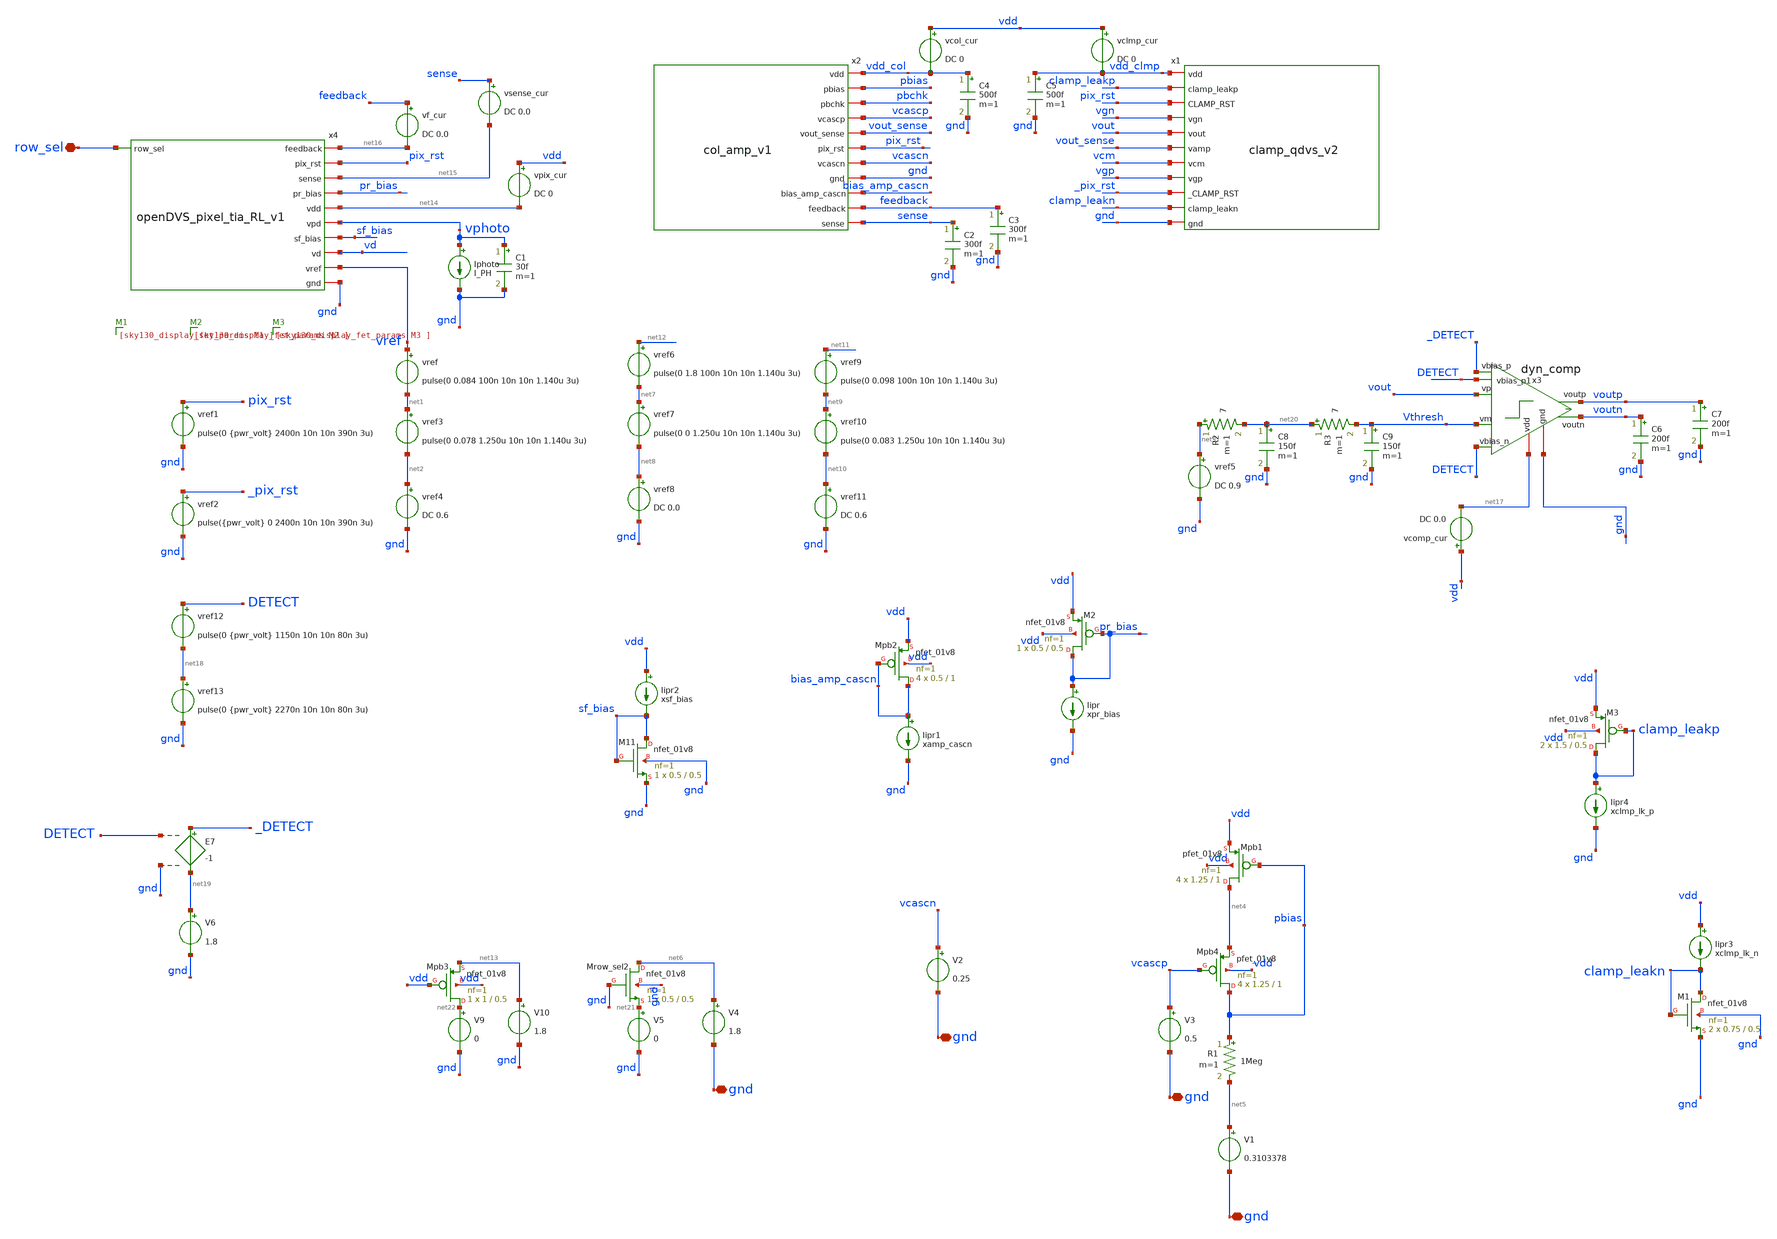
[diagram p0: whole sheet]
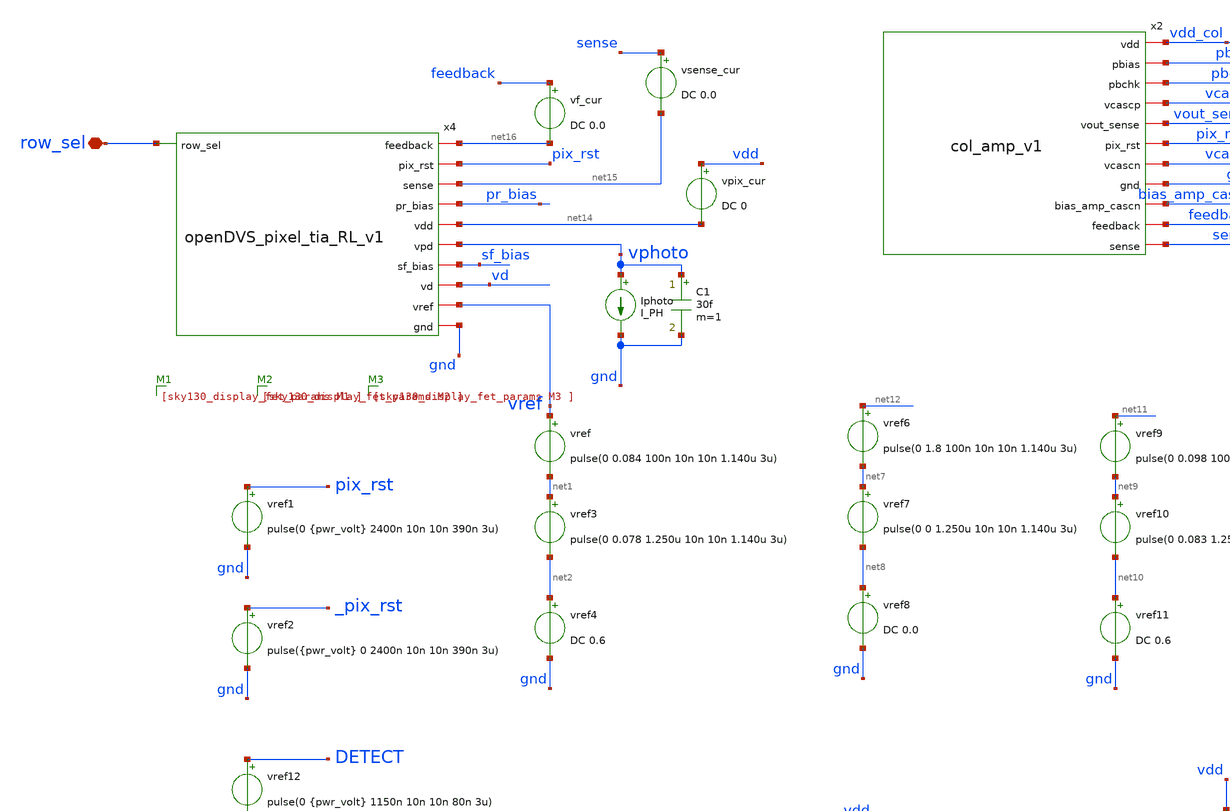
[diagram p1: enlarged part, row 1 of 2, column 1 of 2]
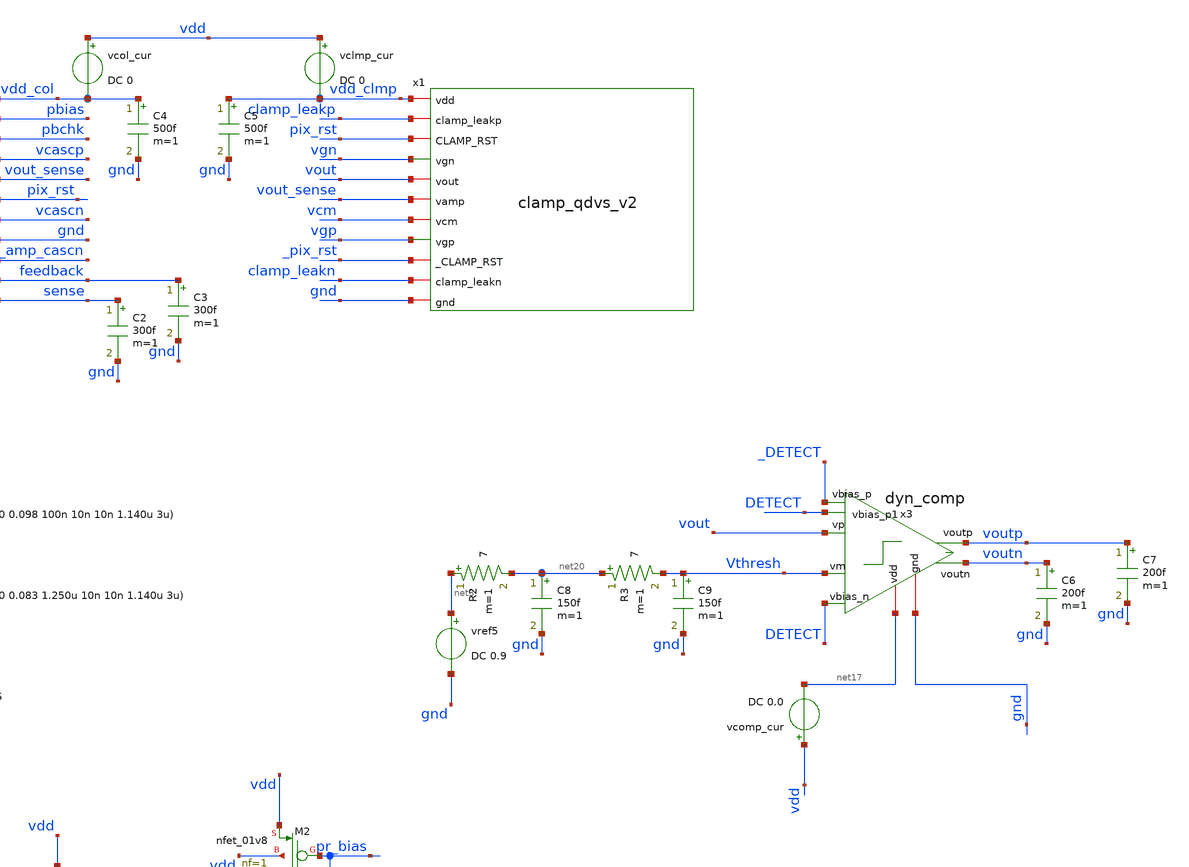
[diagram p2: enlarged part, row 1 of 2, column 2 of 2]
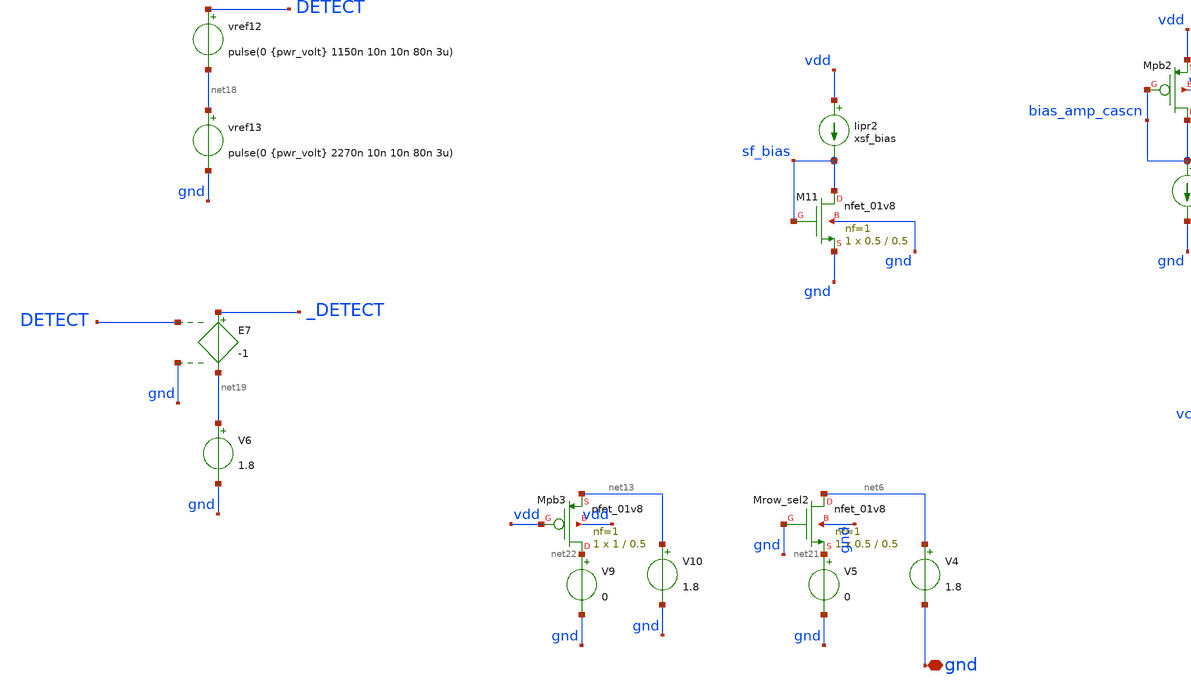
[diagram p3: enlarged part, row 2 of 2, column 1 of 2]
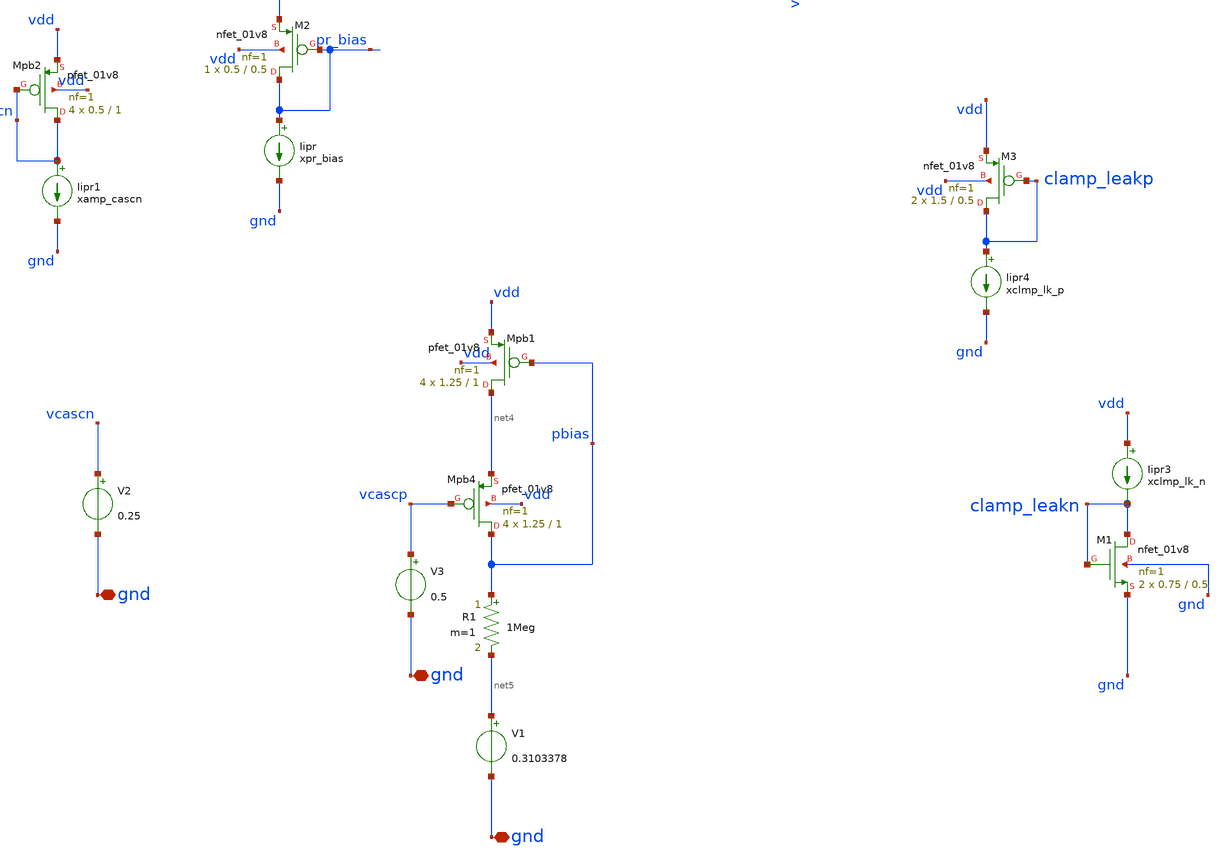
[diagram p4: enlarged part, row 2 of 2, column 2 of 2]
** sch_path: analog/xschem/col_amp_n_clamp_v1/tran_col_pix.sch
**.subckt tran_col_pix row_sel gnd gnd gnd gnd
*.iopin row_sel
*.iopin gnd
*.iopin gnd
*.iopin gnd
*.iopin gnd
C1 vphoto gnd 30f m=1
vref vref net1 pulse(0 0.084 100n 10n 10n 1.140u 3u)
Iphoto vphoto gnd I_PH
vref1 pix_rst gnd pulse(0 {pwr_volt} 2400n 10n 10n 390n 3u)
vref3 net1 net2 pulse(0 0.078 1.250u 10n 10n 1.140u 3u)
vref4 net2 gnd DC 0.6
C2 sense gnd 300f m=1
C3 feedback gnd 300f m=1
XMpb2 bias_amp_cascn bias_amp_cascn vdd vdd sky130_fd_pr__pfet_01v8 L=1 W=0.5 nf=1 ad='int((1 + 1)/2) * 0.5 / 1 * 0.29'
+ as='int((1 + 2)/2) * 0.5 / 1 * 0.29' pd='2*int((1 + 1)/2) * (0.5 / 1 + 0.29)' ps='2*int((1 + 2)/2) * (0.5 / 1 + 0.29)'
+ nrd='0.29 / 0.5 ' nrs='0.29 / 0.5 ' sa=0 sb=0 sd=0 mult=4 m=4
XM11 sf_bias sf_bias gnd gnd sky130_fd_pr__nfet_01v8 L=0.5 W=0.5 nf=1 ad='int((1 + 1)/2) * 0.5 / 1 * 0.29'
+ as='int((1 + 2)/2) * 0.5 / 1 * 0.29' pd='2*int((1 + 1)/2) * (0.5 / 1 + 0.29)' ps='2*int((1 + 2)/2) * (0.5 / 1 + 0.29)'
+ nrd='0.29 / 0.5 ' nrs='0.29 / 0.5 ' sa=0 sb=0 sd=0 mult=1 m=1
vcol_cur vdd vdd_col DC 0
.save i(vcol_cur)
vclmp_cur vdd vdd_clmp DC 0
.save i(vclmp_cur)
C4 vdd_col gnd 500f m=1
C5 vdd_clmp gnd 500f m=1
vref2 _pix_rst gnd pulse({pwr_volt} 0 2400n 10n 10n 390n 3u)
vref5 net3 gnd DC 0.9
XMpb1 net4 pbias vdd vdd sky130_fd_pr__pfet_01v8 L=1 W=1.25 nf=1 ad='int((1 + 1)/2) * 1.25 / 1 * 0.29'
+ as='int((1 + 2)/2) * 1.25 / 1 * 0.29' pd='2*int((1 + 1)/2) * (1.25 / 1 + 0.29)' ps='2*int((1 + 2)/2) * (1.25 / 1 + 0.29)'
+ nrd='0.29 / 1.25 ' nrs='0.29 / 1.25 ' sa=0 sb=0 sd=0 mult=4 m=4
R1 pbias net5 1Meg m=1
V1 net5 gnd 0.3103378
.save i(v1)
XMpb4 pbias vcascp net4 vdd sky130_fd_pr__pfet_01v8 L=1 W=1.25 nf=1 ad='int((1 + 1)/2) * 1.25 / 1 * 0.29'
+ as='int((1 + 2)/2) * 1.25 / 1 * 0.29' pd='2*int((1 + 1)/2) * (1.25 / 1 + 0.29)' ps='2*int((1 + 2)/2) * (1.25 / 1 + 0.29)'
+ nrd='0.29 / 1.25 ' nrs='0.29 / 1.25 ' sa=0 sb=0 sd=0 mult=4 m=4
V3 vcascp gnd 0.5
.save i(v3)
V2 vcascn gnd 0.25
.save i(v2)
XMrow_sel2 net6 gnd net21 gnd sky130_fd_pr__nfet_01v8 L=0.5 W=0.5 nf=1 ad='int((1 + 1)/2) * 0.5 / 1 * 0.29'
+ as='int((1 + 2)/2) * 0.5 / 1 * 0.29' pd='2*int((1 + 1)/2) * (0.5 / 1 + 0.29)' ps='2*int((1 + 2)/2) * (0.5 / 1 + 0.29)'
+ nrd='0.29 / 0.5 ' nrs='0.29 / 0.5 ' sa=0 sb=0 sd=0 mult=1 m=1
V4 net6 gnd 1.8
.save i(v4)
V5 net21 gnd 0
.save i(v5)
vref6 net12 net7 pulse(0 1.8 100n 10n 10n 1.140u 3u)
vref7 net7 net8 pulse(0 0 1.250u 10n 10n 1.140u 3u)
vref8 net8 gnd DC 0.0
vref9 net11 net9 pulse(0 0.098 100n 10n 10n 1.140u 3u)
vref10 net9 net10 pulse(0 0.083 1.250u 10n 10n 1.140u 3u)
vref11 net10 gnd DC 0.6
XMpb3 net22 vdd net13 vdd sky130_fd_pr__pfet_01v8 L=0.5 W=1 nf=1 ad='int((1 + 1)/2) * 1 / 1 * 0.29' as='int((1 + 2)/2) * 1 / 1 * 0.29'
+ pd='2*int((1 + 1)/2) * (1 / 1 + 0.29)' ps='2*int((1 + 2)/2) * (1 / 1 + 0.29)' nrd='0.29 / 1 ' nrs='0.29 / 1 '
+ sa=0 sb=0 sd=0 mult=1 m=1
V9 net22 gnd 0
.save i(v9)
V10 net13 gnd 1.8
.save i(v10)
x2 vdd_col pbias pbchk vcascp vout_sense pix_rst vcascn gnd bias_amp_cascn feedback sense col_amp_v1
x1 vdd_clmp clamp_leakp pix_rst vgn vout vout_sense vcm vgp _pix_rst clamp_leakn gnd clamp_qdvs_v2
vpix_cur vdd net14 DC 0
.save i(vpix_cur)
XM2 pr_bias pr_bias vdd vdd sky130_fd_pr__nfet_01v8 L=0.5 W=0.5 nf=1 ad='int((1 + 1)/2) * 0.5 / 1 * 0.29'
+ as='int((1 + 2)/2) * 0.5 / 1 * 0.29' pd='2*int((1 + 1)/2) * (0.5 / 1 + 0.29)' ps='2*int((1 + 2)/2) * (0.5 / 1 + 0.29)'
+ nrd='0.29 / 0.5 ' nrs='0.29 / 0.5 ' sa=0 sb=0 sd=0 mult=1 m=1
Iipr pr_bias gnd xpr_bias
Iipr1 bias_amp_cascn gnd xamp_cascn
Iipr2 vdd sf_bias xsf_bias
x3 net17 vout Vthresh gnd _DETECT DETECT voutp voutn DETECT dyn_comp
vref12 DETECT net18 pulse(0 {pwr_volt} 1150n 10n 10n 80n 3u)
vref13 net18 gnd pulse(0 {pwr_volt} 2270n 10n 10n 80n 3u)
XM3 clamp_leakp clamp_leakp vdd vdd sky130_fd_pr__nfet_01v8 L=0.5 W=1.5 nf=1 ad='int((1 + 1)/2) * 1.5 / 1 * 0.29'
+ as='int((1 + 2)/2) * 1.5 / 1 * 0.29' pd='2*int((1 + 1)/2) * (1.5 / 1 + 0.29)' ps='2*int((1 + 2)/2) * (1.5 / 1 + 0.29)'
+ nrd='0.29 / 1.5 ' nrs='0.29 / 1.5 ' sa=0 sb=0 sd=0 mult=2 m=2
Iipr4 clamp_leakp gnd xclmp_lk_p
XM1 clamp_leakn clamp_leakn gnd gnd sky130_fd_pr__nfet_01v8 L=0.5 W=0.75 nf=1 ad='int((1 + 1)/2) * 0.75 / 1 * 0.29'
+ as='int((1 + 2)/2) * 0.75 / 1 * 0.29' pd='2*int((1 + 1)/2) * (0.75 / 1 + 0.29)' ps='2*int((1 + 2)/2) * (0.75 / 1 + 0.29)'
+ nrd='0.29 / 0.75 ' nrs='0.29 / 0.75 ' sa=0 sb=0 sd=0 mult=2 m=2
Iipr3 vdd clamp_leakn xclmp_lk_n
E7 _DETECT net19 DETECT gnd -1
V6 net19 gnd 1.8
.save i(v6)
vcomp_cur vdd net17 DC 0.0
.save i(vcomp_cur)
C6 voutn gnd 200f m=1
C7 voutp gnd 200f m=1
vf_cur feedback net16 DC 0.0
.save i(vf_cur)
vsense_cur sense net15 DC 0.0
.save i(vsense_cur)
R2 net3 net20 7 m=1
C8 net20 gnd 150f m=1
R3 net20 Vthresh 7 m=1
C9 Vthresh gnd 150f m=1
x4 net16 pix_rst net15 row_sel pr_bias net14 vphoto sf_bias vd vref gnd openDVS_pixel_tia_RL_v1
**** begin user architecture code

** opencircuitdesign pdks install
.lib $::SKYWATER_MODELS/sky130.lib.spice tt




Vvdd vdd gnd DC pwr_volt

*Bias Setting
.param xpr_bias=10n
.param xsf_bias=5n
.param xamp_cascn=200n
.param xclmp_lk_p=10p
.param xclmp_lk_n=10p
.param xpix_rst_bias=100n
.param I_PH = 0
.param pwr_volt = 1.8

*Small Iphoto testing
Iphoto1 vphoto gnd pulse(50n 60n 12u 5n 5n 5.99u 30u)
Iphoto2 vphoto gnd pulse(50n 40n 24u 5n 5n 5.99u 30u)

*large Iphoto testing
*Iphoto1 vphoto gnd pulse(5n 5u 12u 5n 5n 5.99u 30u)
*Iphoto2 vphoto gnd pulse(5n 5p 24u 5n 5n 5.99u 30u)

Vrow row_sel gnd DC pwr_volt
Vvcm vcm gnd DC 0.9

.option gmin=1e-15 abstol=1e-15 vntol=1e-9 reltol=1e-6 chgtol=1e-16 trtol=6

.control

	save all
	op
	tran 0.2n 39u
	plot v(vphoto) v(vph_sf) v(vin) v(vout_sense) v(vref) v(vcmp) v(vcm) v(vout)


	write tran_col_pix.raw
.endc


**** end user architecture code
**.ends
.end
